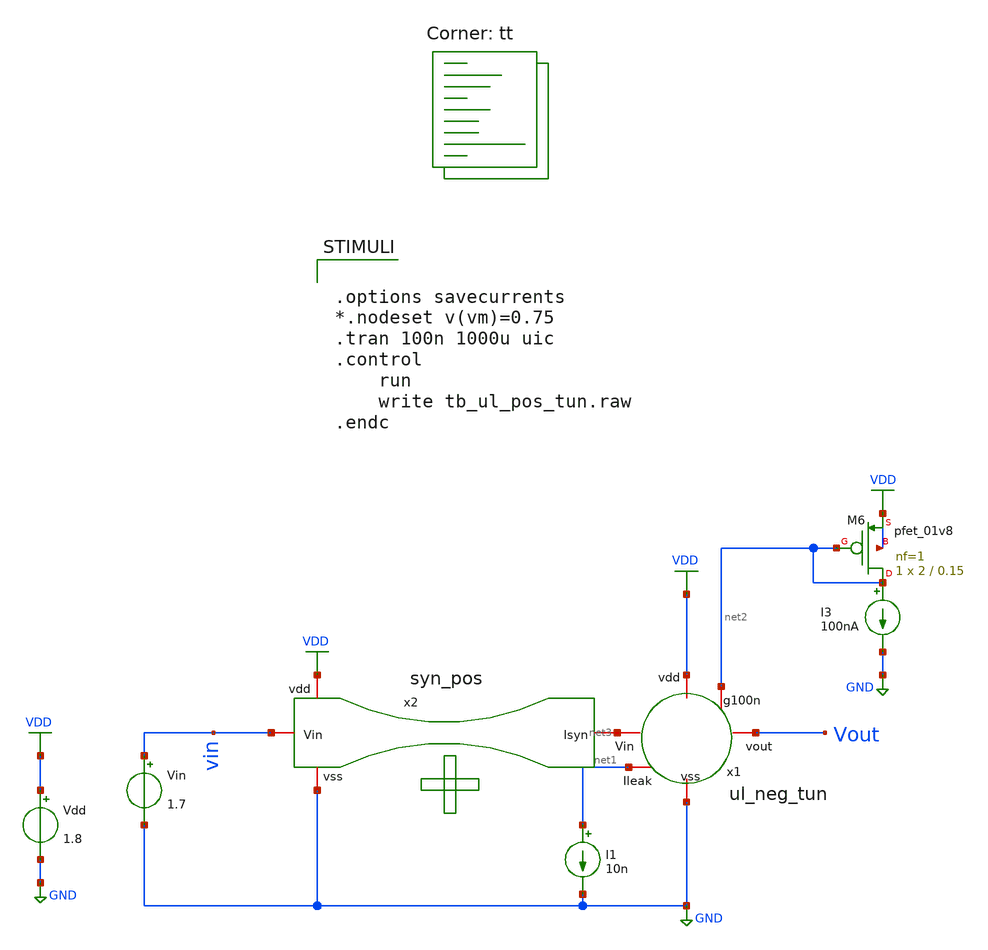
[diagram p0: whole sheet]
** sch_path: Neuron/ultralif/tb_ul_pos_tun.sch
**.subckt tb_ul_pos_tun
I1 net1 GND 10n
Vdd VDD GND 1.8
I3 net2 GND 100nA
Vin vin GND 1.7
XM6 net2 net2 VDD VDD sky130_fd_pr__pfet_01v8 L=0.15 W=2 nf=1 ad='int((nf+1)/2) * W/nf * 0.29' as='int((nf+2)/2) * W/nf * 0.29'
+ pd='2*int((nf+1)/2) * (W/nf + 0.29)' ps='2*int((nf+2)/2) * (W/nf + 0.29)' nrd='0.29 / W' nrs='0.29 / W'
+ sa=0 sb=0 sd=0 mult=1 m=1
x1 net3 VDD net2 Vout net1 GND ul_neg_tun
x2 GND vin net3 VDD syn_pos
**** begin user architecture code
.lib $::SKYWATER_MODELS/sky130.lib.spice tt
**** end user architecture code
**.ends

* expanding   symbol:  ul_neg_tun.sym # of pins=6
** sym_path: Neuron/ultralif/ul_neg_tun.sym
** sch_path: Neuron/ultralif/ul_neg_tun.sch
.subckt ul_neg_tun Iext vdd g100n vout Ileak vss
*.iopin Iext
*.iopin vout
*.iopin vss
*.iopin Ileak
*.iopin vdd
*.iopin g100n
XM1 Ileak Ileak vm vdd sky130_fd_pr__pfet_01v8 L=10 W=1 nf=1 ad='int((nf+1)/2) * W/nf * 0.29' as='int((nf+2)/2) * W/nf * 0.29'
+ pd='2*int((nf+1)/2) * (W/nf + 0.29)' ps='2*int((nf+2)/2) * (W/nf + 0.29)' nrd='0.29 / W' nrs='0.29 / W'
+ sa=0 sb=0 sd=0 mult=1 m=1
XM2 Ileak net1 vm vdd sky130_fd_pr__pfet_01v8 L=0.15 W=1.5 nf=1 ad='int((nf+1)/2) * W/nf * 0.29' as='int((nf+2)/2) * W/nf * 0.29'
+ pd='2*int((nf+1)/2) * (W/nf + 0.29)' ps='2*int((nf+2)/2) * (W/nf + 0.29)' nrd='0.29 / W' nrs='0.29 / W'
+ sa=0 sb=0 sd=0 mult=1 m=1
XM3 net1 net1 vm vdd sky130_fd_pr__pfet_01v8 L=0.15 W=15 nf=1 ad='int((nf+1)/2) * W/nf * 0.29' as='int((nf+2)/2) * W/nf * 0.29'
+ pd='2*int((nf+1)/2) * (W/nf + 0.29)' ps='2*int((nf+2)/2) * (W/nf + 0.29)' nrd='0.29 / W' nrs='0.29 / W'
+ sa=0 sb=0 sd=0 mult=1 m=1
XM4 net1 Ileak vss vss sky130_fd_pr__nfet_01v8 L=4 W=1 nf=1 ad='int((1 + 1)/2) * 1 / 1 * 0.29' as='int((1 + 2)/2) * 1 / 1 * 0.29'
+ pd='2*int((1 + 1)/2) * (1 / 1 + 0.29)' ps='2*int((1 + 2)/2) * (1 / 1 + 0.29)' nrd='0.29 / 1 ' nrs='0.29 / 1 '
+ sa=0 sb=0 sd=0 mult=1 m=1
C1 vm vss 1p m=1
XM5 vout_n Ileak vss vss sky130_fd_pr__nfet_01v8 L=0.15 W=1 nf=1 ad='int((1 + 1)/2) * 1 / 1 * 0.29' as='int((1 + 2)/2) * 1 / 1 * 0.29'
+ pd='2*int((1 + 1)/2) * (1 / 1 + 0.29)' ps='2*int((1 + 2)/2) * (1 / 1 + 0.29)' nrd='0.29 / 1 ' nrs='0.29 / 1 '
+ sa=0 sb=0 sd=0 mult=1 m=1
XM6 vout_n g100n vdd vdd sky130_fd_pr__pfet_01v8 L=0.15 W=2 nf=1 ad='int((nf+1)/2) * W/nf * 0.29' as='int((nf+2)/2) * W/nf * 0.29'
+ pd='2*int((nf+1)/2) * (W/nf + 0.29)' ps='2*int((nf+2)/2) * (W/nf + 0.29)' nrd='0.29 / W' nrs='0.29 / W'
+ sa=0 sb=0 sd=0 mult=1 m=1
XM7 vout vout_n vss vss sky130_fd_pr__nfet_01v8 L=0.15 W=1 nf=1 ad='int((1 + 1)/2) * 1 / 1 * 0.29' as='int((1 + 2)/2) * 1 / 1 * 0.29'
+ pd='2*int((1 + 1)/2) * (1 / 1 + 0.29)' ps='2*int((1 + 2)/2) * (1 / 1 + 0.29)' nrd='0.29 / 1 ' nrs='0.29 / 1 '
+ sa=0 sb=0 sd=0 mult=1 m=1
XM8 vout vout_n vdd vdd sky130_fd_pr__pfet_01v8 L=0.15 W=2 nf=1 ad='int((nf+1)/2) * W/nf * 0.29' as='int((nf+2)/2) * W/nf * 0.29'
+ pd='2*int((nf+1)/2) * (W/nf + 0.29)' ps='2*int((nf+2)/2) * (W/nf + 0.29)' nrd='0.29 / W' nrs='0.29 / W'
+ sa=0 sb=0 sd=0 mult=1 m=1
XM9 vm Ileak Iext vdd sky130_fd_pr__pfet_01v8 L=0.15 W=2 nf=1 ad='int((nf+1)/2) * W/nf * 0.29' as='int((nf+2)/2) * W/nf * 0.29'
+ pd='2*int((nf+1)/2) * (W/nf + 0.29)' ps='2*int((nf+2)/2) * (W/nf + 0.29)' nrd='0.29 / W' nrs='0.29 / W'
+ sa=0 sb=0 sd=0 mult=1 m=1
.ends


* expanding   symbol:  syn_pos.sym # of pins=4
** sym_path: Neuron/ultralif/syn_pos.sym
** sch_path: Neuron/ultralif/syn_pos.sch
.subckt syn_pos vss Vin Isyn vdd
*.iopin Vin
*.iopin vdd
*.iopin vss
*.iopin Isyn
XM9 Isyn vx vdd vdd sky130_fd_pr__pfet_01v8 L=1 W=0.5 nf=1 ad='int((nf+1)/2) * W/nf * 0.29' as='int((nf+2)/2) * W/nf * 0.29'
+ pd='2*int((nf+1)/2) * (W/nf + 0.29)' ps='2*int((nf+2)/2) * (W/nf + 0.29)' nrd='0.29 / W' nrs='0.29 / W'
+ sa=0 sb=0 sd=0 mult=1 m=1
XM10 vx vx vdd vdd sky130_fd_pr__pfet_01v8 L=0.15 W=0.5 nf=1 ad='int((nf+1)/2) * W/nf * 0.29' as='int((nf+2)/2) * W/nf * 0.29'
+ pd='2*int((nf+1)/2) * (W/nf + 0.29)' ps='2*int((nf+2)/2) * (W/nf + 0.29)' nrd='0.29 / W' nrs='0.29 / W'
+ sa=0 sb=0 sd=0 mult=5 m=5
XM12 vx Vin vss vss sky130_fd_pr__nfet_01v8 L=1 W=0.4 nf=1 ad='int((1 + 1)/2) * 0.4 / 1 * 0.29' as='int((1 + 2)/2) * 0.4 / 1 * 0.29'
+ pd='2*int((1 + 1)/2) * (0.4 / 1 + 0.29)' ps='2*int((1 + 2)/2) * (0.4 / 1 + 0.29)' nrd='0.29 / 0.4 ' nrs='0.29 / 0.4 '
+ sa=0 sb=0 sd=0 mult=1 m=1
.ends

.GLOBAL GND
.GLOBAL VDD
**** begin user architecture code


.options savecurrents
*.nodeset v(vm)=0.75
.tran 100n 1000u uic
.control
	run
	write tb_ul_pos_tun.raw
.endc


**** end user architecture code
.end
